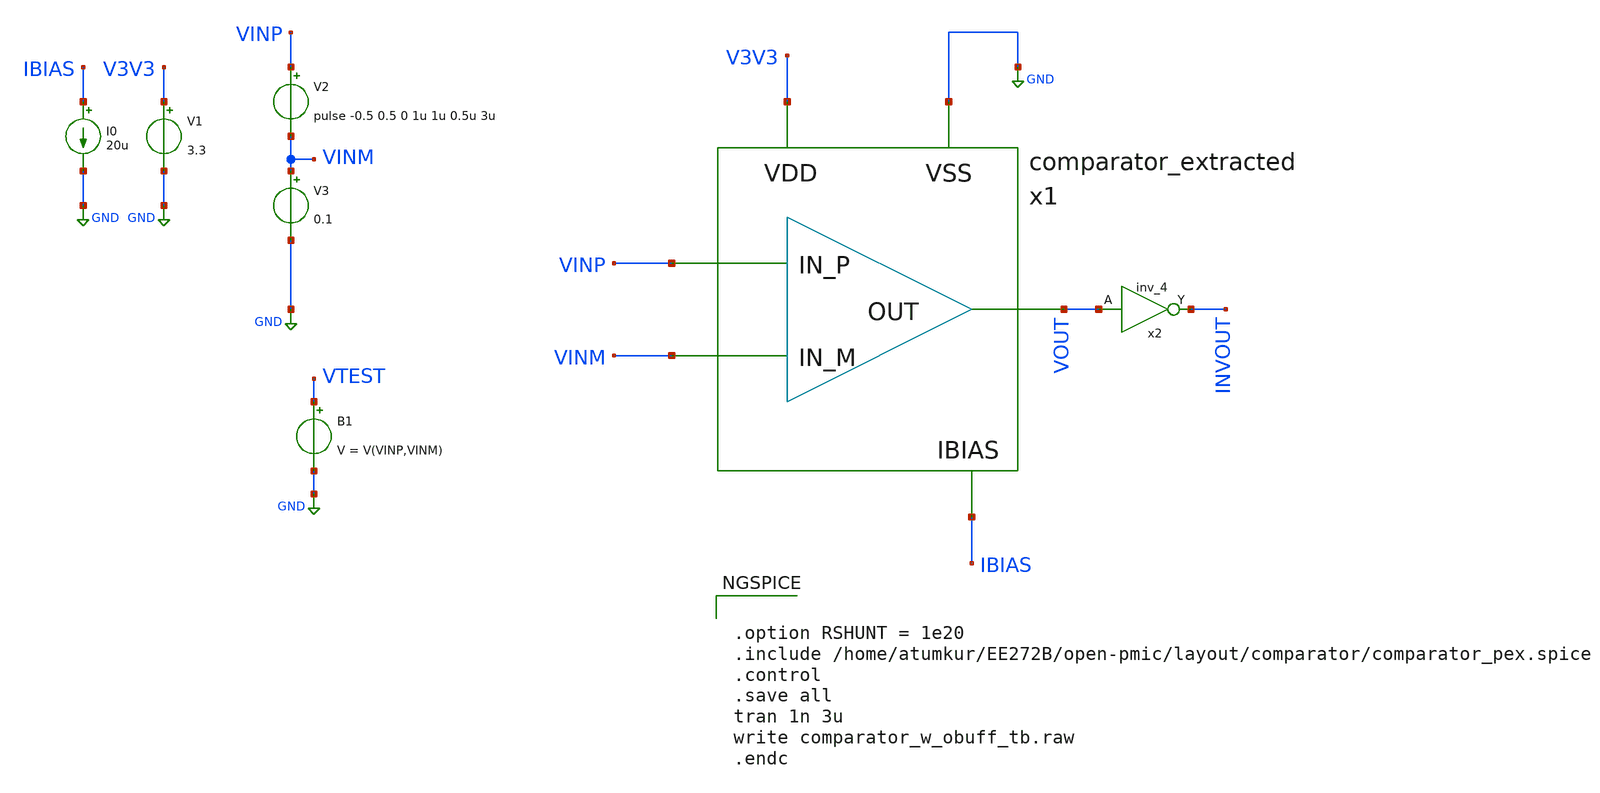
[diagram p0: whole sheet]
** sch_path: images/iic-osic-tools/addons/examples/open-pmic/layout/comparator/comparator_w_obuff_tb.sch
**.subckt comparator_w_obuff_tb
V1 V3V3 GND 3.3
I0 IBIAS GND 20u
V3 VINM GND 0.1
x2 VOUT GND GND V3V3 V3V3 INVOUT sky130_fd_sc_hvl__inv_4
B1 VTEST GND V = V(VINP,VINM)
x1 IBIAS V3V3 VINM VINP VOUT GND comparator_extracted
V2 VINP VINM pulse -0.5 0.5 0 1u 1u 0.5u 3u
**** begin user architecture code

.include $::SKYWATER_MODELS/cells/nfet_01v8/sky130_fd_pr__nfet_01v8__tt.corner.spice
.include $::SKYWATER_MODELS/cells/nfet_01v8_lvt/sky130_fd_pr__nfet_01v8_lvt__tt.corner.spice
.include $::SKYWATER_MODELS/cells/pfet_01v8/sky130_fd_pr__pfet_01v8__tt.corner.spice
.include $::SKYWATER_MODELS/cells/nfet_03v3_nvt/sky130_fd_pr__nfet_03v3_nvt__tt.corner.spice
.include $::SKYWATER_MODELS/cells/nfet_05v0_nvt/sky130_fd_pr__nfet_05v0_nvt__tt.corner.spice
.include $::SKYWATER_MODELS/cells/esd_nfet_01v8/sky130_fd_pr__esd_nfet_01v8__tt.corner.spice
.include $::SKYWATER_MODELS/cells/pfet_01v8_lvt/sky130_fd_pr__pfet_01v8_lvt__tt.corner.spice
.include $::SKYWATER_MODELS/cells/pfet_01v8_hvt/sky130_fd_pr__pfet_01v8_hvt__tt.corner.spice
.include $::SKYWATER_MODELS/cells/esd_pfet_g5v0d10v5/sky130_fd_pr__esd_pfet_g5v0d10v5__tt.corner.spice
.include $::SKYWATER_MODELS/cells/pfet_g5v0d10v5/sky130_fd_pr__pfet_g5v0d10v5__tt.corner.spice
.include $::SKYWATER_MODELS/cells/pfet_g5v0d16v0/sky130_fd_pr__pfet_g5v0d16v0__tt.corner.spice
.include $::SKYWATER_MODELS/cells/nfet_g5v0d10v5/sky130_fd_pr__nfet_g5v0d10v5__tt.corner.spice
.include $::SKYWATER_MODELS/cells/nfet_g5v0d16v0/sky130_fd_pr__nfet_g5v0d16v0__tt_discrete.corner.spice
.include $::SKYWATER_MODELS/cells/esd_nfet_g5v0d10v5/sky130_fd_pr__esd_nfet_g5v0d10v5__tt.corner.spice
.include $::SKYWATER_MODELS/models/corners/tt/nonfet.spice
* Mismatch parameters
.include $::SKYWATER_MODELS/cells/nfet_01v8/sky130_fd_pr__nfet_01v8__mismatch.corner.spice
.include $::SKYWATER_MODELS/cells/pfet_01v8/sky130_fd_pr__pfet_01v8__mismatch.corner.spice
.include $::SKYWATER_MODELS/cells/nfet_01v8_lvt/sky130_fd_pr__nfet_01v8_lvt__mismatch.corner.spice
.include $::SKYWATER_MODELS/cells/pfet_01v8_lvt/sky130_fd_pr__pfet_01v8_lvt__mismatch.corner.spice
.include $::SKYWATER_MODELS/cells/pfet_01v8_hvt/sky130_fd_pr__pfet_01v8_hvt__mismatch.corner.spice
.include $::SKYWATER_MODELS/cells/nfet_g5v0d10v5/sky130_fd_pr__nfet_g5v0d10v5__mismatch.corner.spice
.include $::SKYWATER_MODELS/cells/pfet_g5v0d10v5/sky130_fd_pr__pfet_g5v0d10v5__mismatch.corner.spice
.include $::SKYWATER_MODELS/cells/nfet_05v0_nvt/sky130_fd_pr__nfet_05v0_nvt__mismatch.corner.spice
.include $::SKYWATER_MODELS/cells/nfet_03v3_nvt/sky130_fd_pr__nfet_03v3_nvt__mismatch.corner.spice
* Resistor$::SKYWATER_MODELS/Capacitor
.include $::SKYWATER_MODELS/models/r+c/res_typical__cap_typical.spice
.include $::SKYWATER_MODELS/models/r+c/res_typical__cap_typical__lin.spice
* Special cells
.include $::SKYWATER_MODELS/models/corners/tt/specialized_cells.spice
* All models
.include $::SKYWATER_MODELS/models/all.spice
* Corner
.include $::SKYWATER_MODELS/models/corners/tt/rf.spice



.option RSHUNT = 1e20
.include /home/atumkur/EE272B/open-pmic/layout/comparator/comparator_pex.spice
.control
.save all
tran 1n 3u
write comparator_w_obuff_tb.raw
.endc


**** end user architecture code
**.ends
.GLOBAL GND
**** begin user architecture code
[sky130_models]
**** end user architecture code
.end
